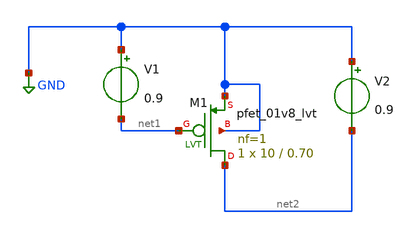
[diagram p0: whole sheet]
** sch_path: MOS-Design-Parameters/PMOS/act6.sch
**.subckt act6
XM1 net2 net1 GND GND sky130_fd_pr__pfet_01v8_lvt L=0.70 W=10 nf=1 ad='int((nf+1)/2) * W/nf * 0.29' as='int((nf+2)/2) * W/nf * 0.29'
+ pd='2*int((nf+1)/2) * (W/nf + 0.29)' ps='2*int((nf+2)/2) * (W/nf + 0.29)' nrd='0.29 / W' nrs='0.29 / W'
+ sa=0 sb=0 sd=0 mult=1 m=1
V1 GND net1 0.9
V2 GND net2 0.9
**** begin user architecture code



.lib /usr/local/share/pdk/sky130A/libs.tech/ngspice/sky130.lib.spice ff
.option wnflag=1 scale=1e-6

.control

save all

save @m.xm1.msky130_fd_pr__pfet_01v8_lvt[id]
save @m.xm1.msky130_fd_pr__pfet_01v8_lvt[gm]


dc v1 -0.2 1.8 1m

let id = @m.xm1.msky130_fd_pr__pfet_01v8_lvt[id]
let gm = @m.xm1.msky130_fd_pr__pfet_01v8_lvt[gm]

let gmoverid = gm/id

#wrdata ftgmid-ss.txt ftgmid vstar

.endc


**** end user architecture code
**.ends
.GLOBAL GND
.end
